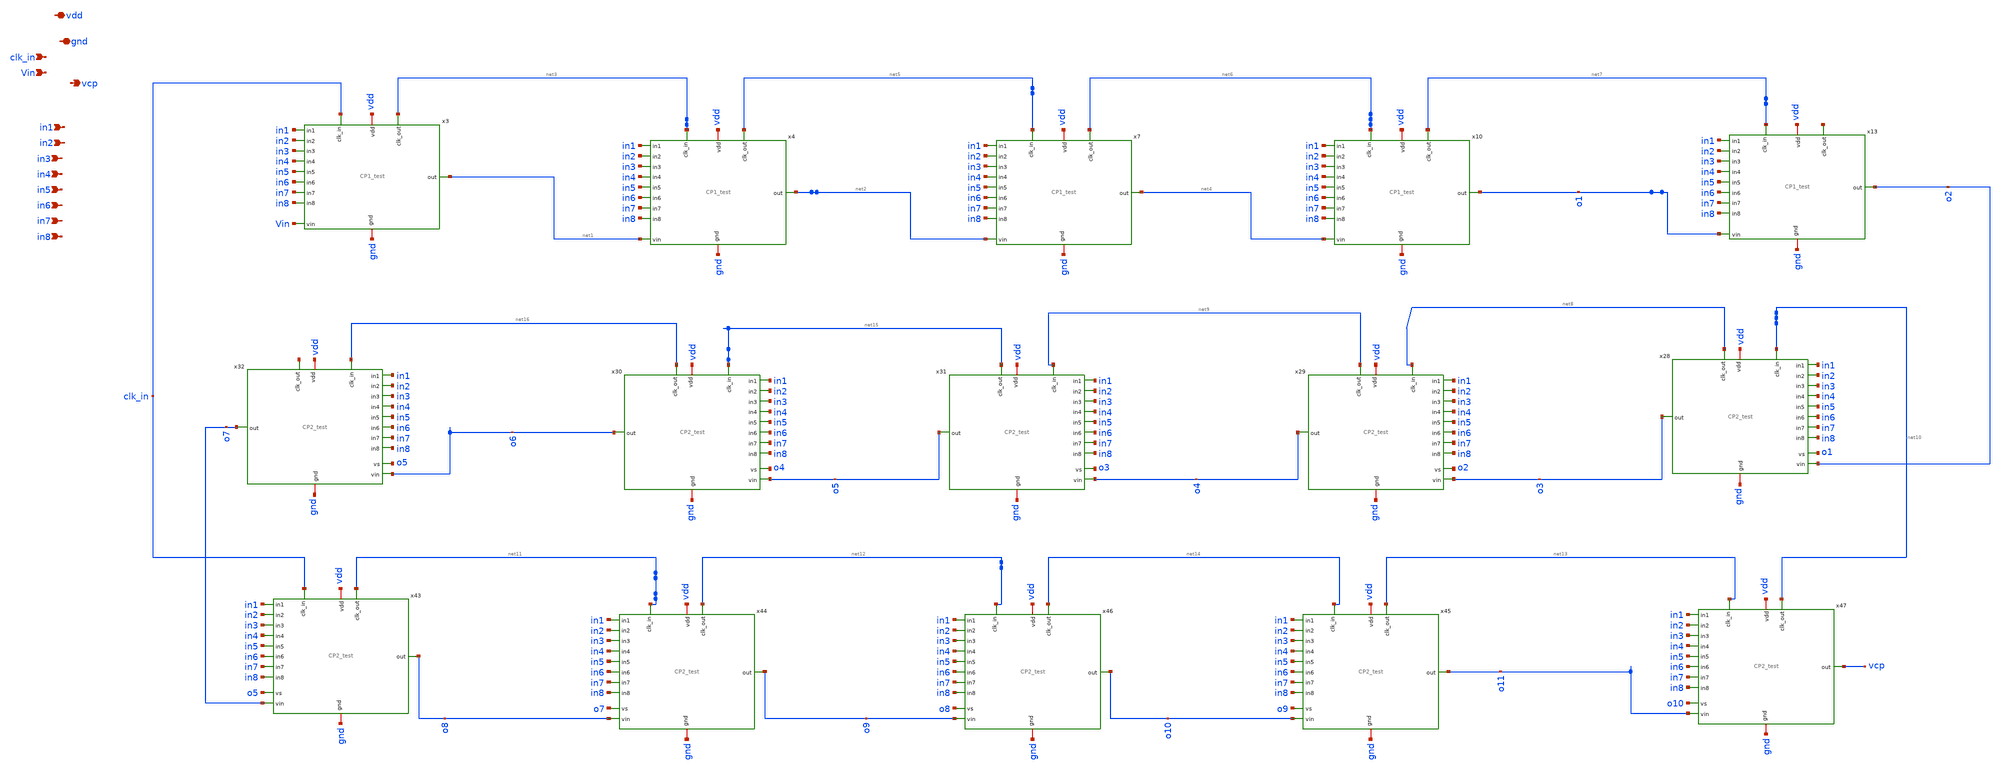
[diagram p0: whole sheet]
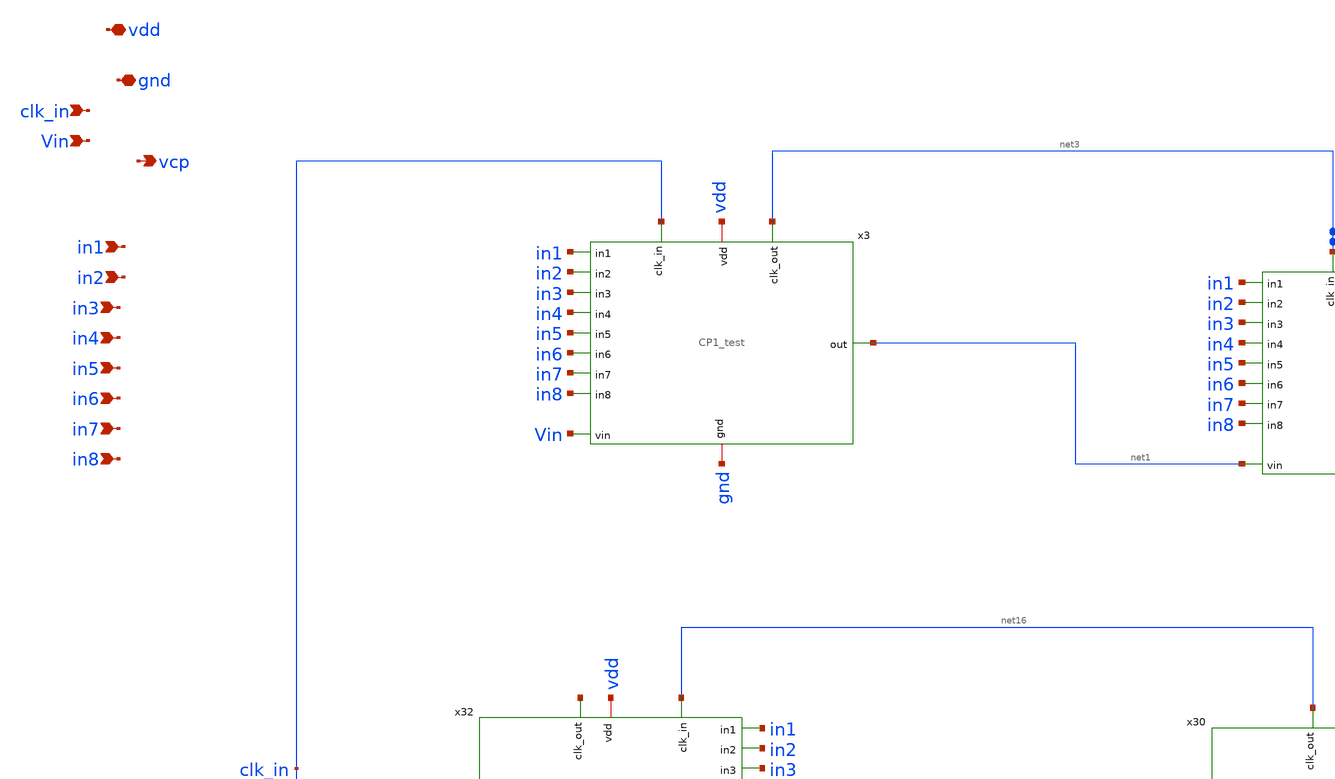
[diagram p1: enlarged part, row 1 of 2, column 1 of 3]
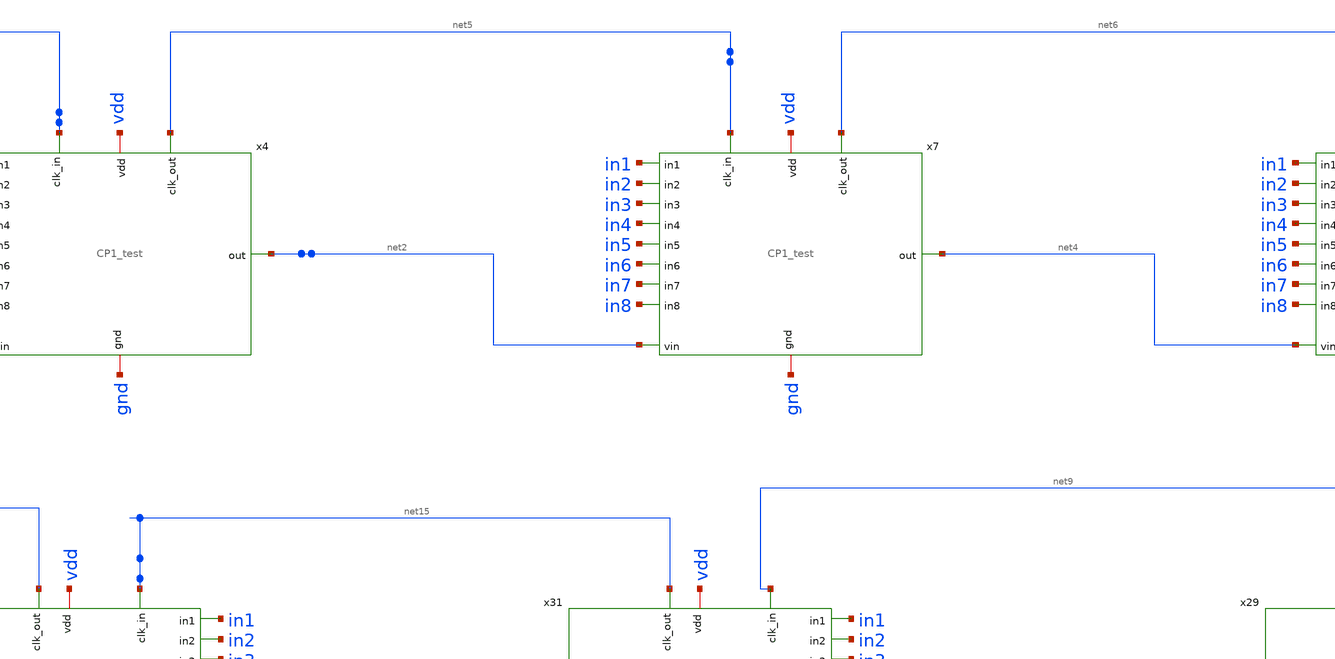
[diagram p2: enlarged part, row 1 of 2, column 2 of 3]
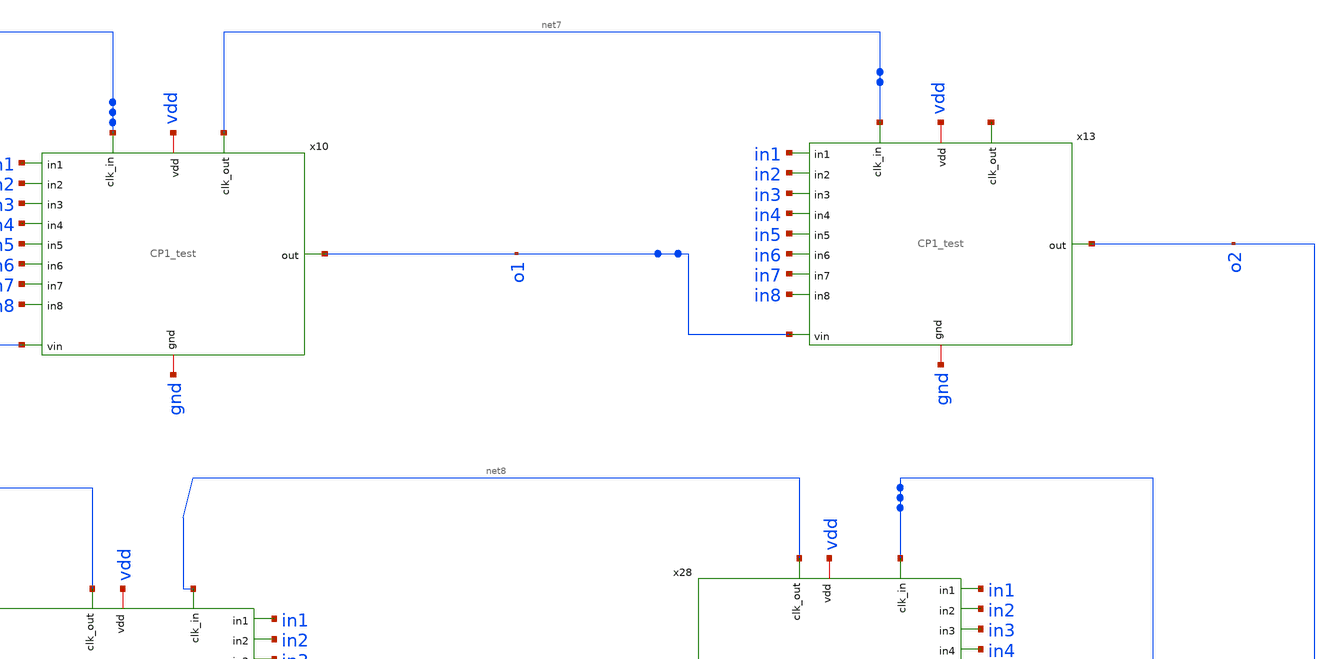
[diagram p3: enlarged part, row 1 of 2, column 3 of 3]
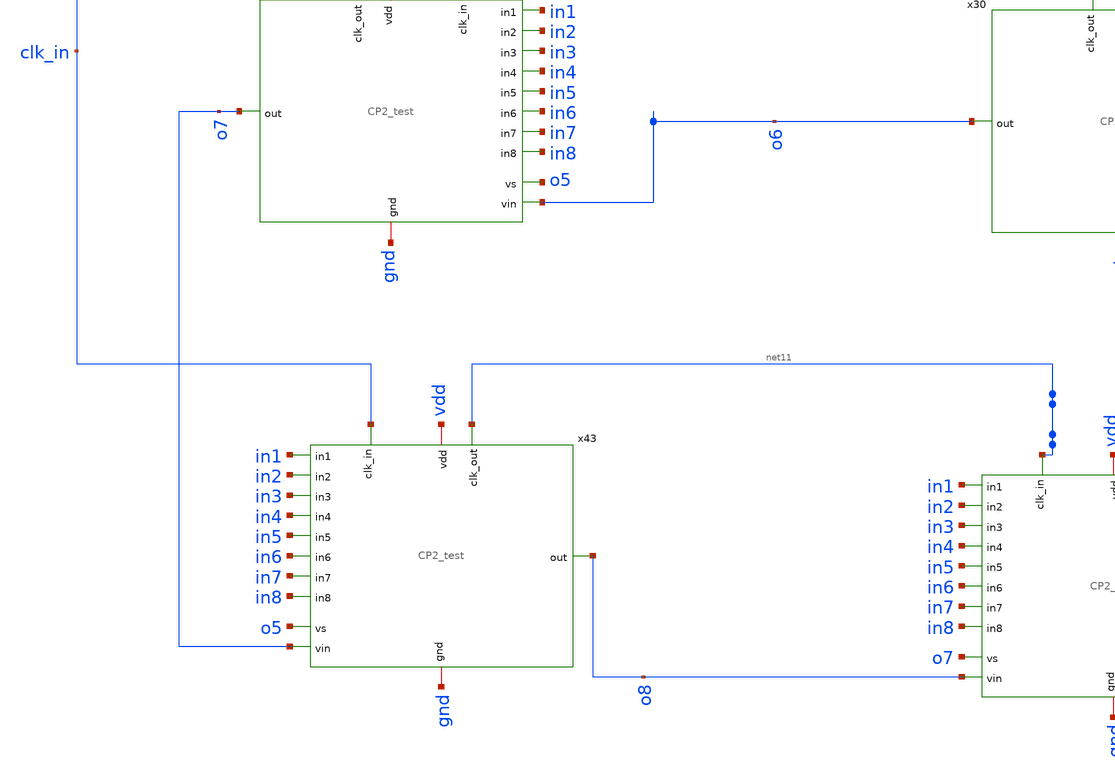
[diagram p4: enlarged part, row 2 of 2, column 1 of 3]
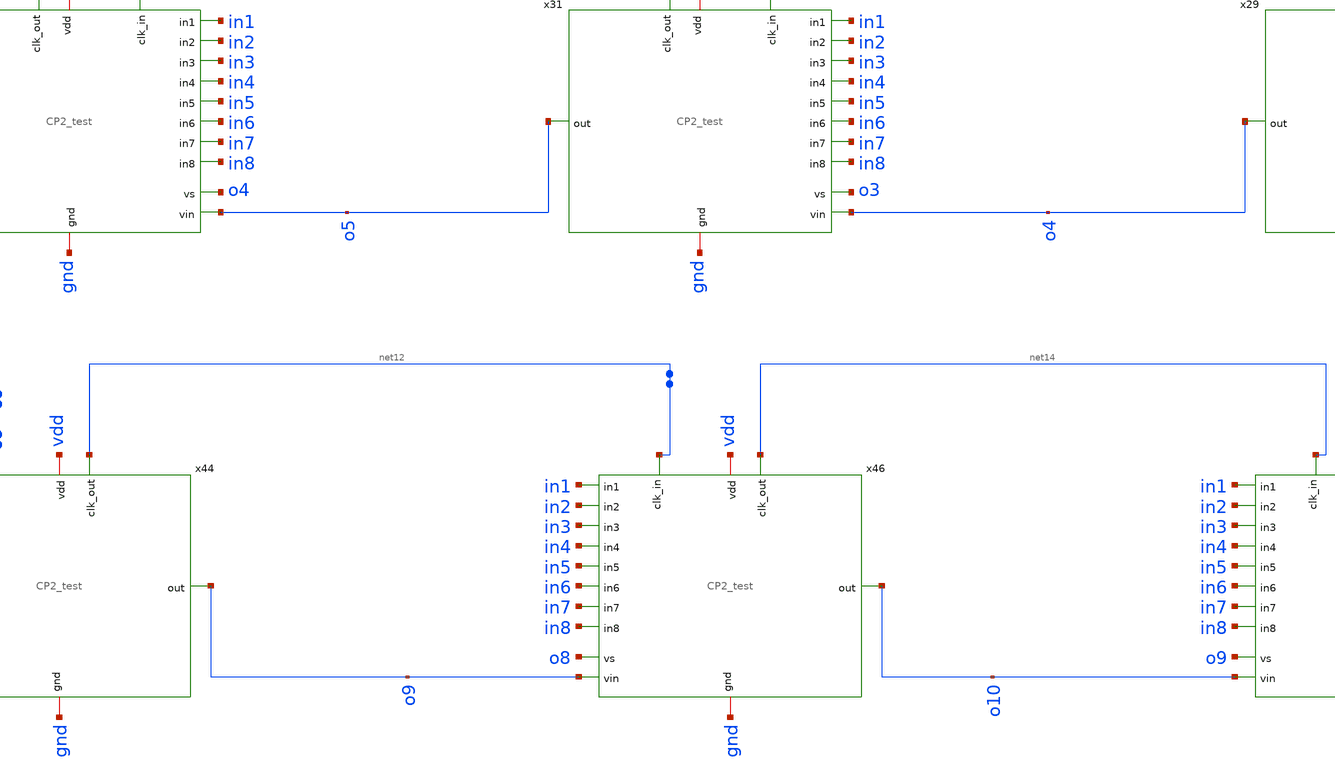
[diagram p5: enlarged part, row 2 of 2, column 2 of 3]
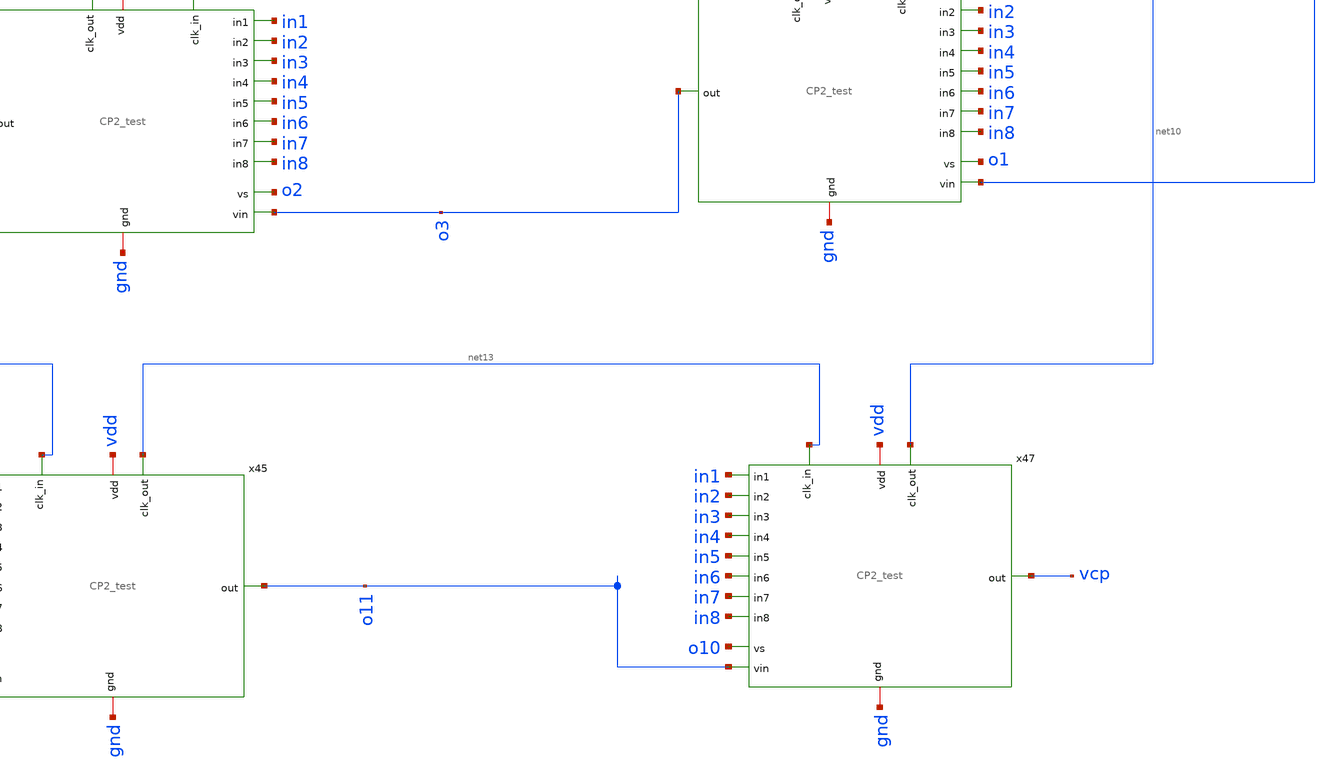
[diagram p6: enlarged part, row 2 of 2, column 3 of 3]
** sch_path: xschem/charge_pumps2/reconfigurable_CP1.sch
**.subckt reconfigurable_CP1 clk_in vdd vcp Vin gnd in1 in2 in3 in4 in5 in6 in7 in8
*.ipin clk_in
*.iopin vdd
*.opin vcp
*.ipin Vin
*.iopin gnd
*.ipin in1
*.ipin in2
*.ipin in3
*.ipin in4
*.ipin in5
*.ipin in6
*.ipin in7
*.ipin in8
x3 gnd clk_in Vin net1 in1 in2 in3 in4 in5 in6 in7 in8 vdd net3 CP1_test
x4 gnd net3 net1 net2 in1 in2 in3 in4 in5 in6 in7 in8 vdd net5 CP1_test
x7 gnd net5 net2 net4 in1 in2 in3 in4 in5 in6 in7 in8 vdd net6 CP1_test
x10 gnd net6 net4 o1 in1 in2 in3 in4 in5 in6 in7 in8 vdd net7 CP1_test
x13 gnd net7 o1 o2 in1 in2 in3 in4 in5 in6 in7 in8 vdd net17 CP1_test
x28 gnd o1 net10 o2 o3 in1 in2 in3 in4 in5 in6 in7 in8 vdd net8 CP2_test
x29 gnd o2 net8 o3 o4 in1 in2 in3 in4 in5 in6 in7 in8 vdd net9 CP2_test
x30 gnd o4 net15 o5 o6 in1 in2 in3 in4 in5 in6 in7 in8 vdd net16 CP2_test
x31 gnd o3 net9 o4 o5 in1 in2 in3 in4 in5 in6 in7 in8 vdd net15 CP2_test
x32 gnd o5 net16 o6 o7 in1 in2 in3 in4 in5 in6 in7 in8 vdd net18 CP2_test
x43 gnd o5 clk_in o7 o8 in1 in2 in3 in4 in5 in6 in7 in8 vdd net11 CP2_test
x44 gnd o7 net11 o8 o9 in1 in2 in3 in4 in5 in6 in7 in8 vdd net12 CP2_test
x45 gnd o9 net14 o10 o11 in1 in2 in3 in4 in5 in6 in7 in8 vdd net13 CP2_test
x46 gnd o8 net12 o9 o10 in1 in2 in3 in4 in5 in6 in7 in8 vdd net14 CP2_test
x47 gnd o10 net13 o11 vcp in1 in2 in3 in4 in5 in6 in7 in8 vdd net10 CP2_test
**.ends
.end
